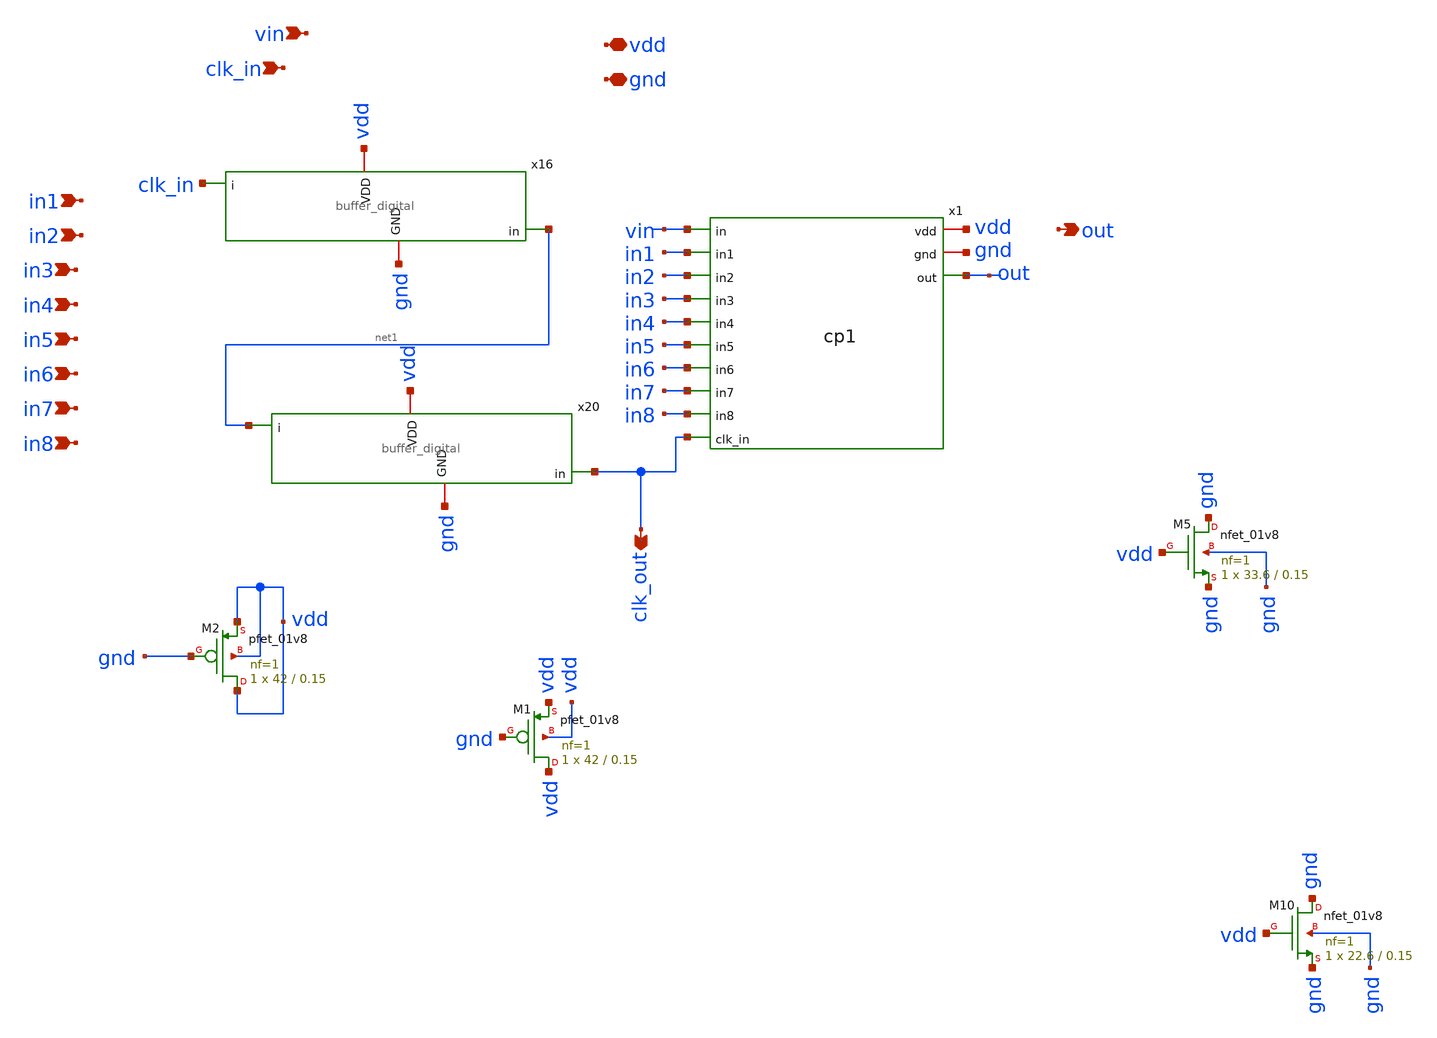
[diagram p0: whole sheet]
** sch_path: xschem/charge_pumps2/cp1_buffer.sch
**.subckt cp1_buffer gnd vdd vin out clk_in in1 in2 in3 in4 in5 in6 in7 in8 clk_out
*.iopin gnd
*.iopin vdd
*.ipin vin
*.opin out
*.ipin clk_in
*.ipin in1
*.ipin in2
*.ipin in3
*.ipin in4
*.ipin in5
*.ipin in6
*.ipin in7
*.ipin in8
*.opin clk_out
x1 vin vdd gnd in1 in2 in3 in4 in5 in6 in7 in8 clk_out out cp1
x16 gnd vdd clk_in net1 buffer_digital
x20 gnd vdd net1 clk_out buffer_digital
XM1 vdd gnd vdd vdd sky130_fd_pr__pfet_01v8 L=0.15 W=42 nf=1 ad='int((nf+1)/2) * W/nf * 0.29' as='int((nf+2)/2) * W/nf * 0.29'
+ pd='2*int((nf+1)/2) * (W/nf + 0.29)' ps='2*int((nf+2)/2) * (W/nf + 0.29)' nrd='0.29 / W' nrs='0.29 / W'
+ sa=0 sb=0 sd=0 mult=1 m=1
XM5 gnd vdd gnd gnd sky130_fd_pr__nfet_01v8 L=0.15 W=33.6 nf=1 ad='int((nf+1)/2) * W/nf * 0.29' as='int((nf+2)/2) * W/nf * 0.29'
+ pd='2*int((nf+1)/2) * (W/nf + 0.29)' ps='2*int((nf+2)/2) * (W/nf + 0.29)' nrd='0.29 / W' nrs='0.29 / W'
+ sa=0 sb=0 sd=0 mult=1 m=1
XM10 gnd vdd gnd gnd sky130_fd_pr__nfet_01v8 L=0.15 W=22.6 nf=1 ad='int((nf+1)/2) * W/nf * 0.29' as='int((nf+2)/2) * W/nf * 0.29'
+ pd='2*int((nf+1)/2) * (W/nf + 0.29)' ps='2*int((nf+2)/2) * (W/nf + 0.29)' nrd='0.29 / W' nrs='0.29 / W'
+ sa=0 sb=0 sd=0 mult=1 m=1
XM2 vdd gnd vdd vdd sky130_fd_pr__pfet_01v8 L=0.15 W=42 nf=1 ad='int((nf+1)/2) * W/nf * 0.29' as='int((nf+2)/2) * W/nf * 0.29'
+ pd='2*int((nf+1)/2) * (W/nf + 0.29)' ps='2*int((nf+2)/2) * (W/nf + 0.29)' nrd='0.29 / W' nrs='0.29 / W'
+ sa=0 sb=0 sd=0 mult=1 m=1
**.ends
.end
